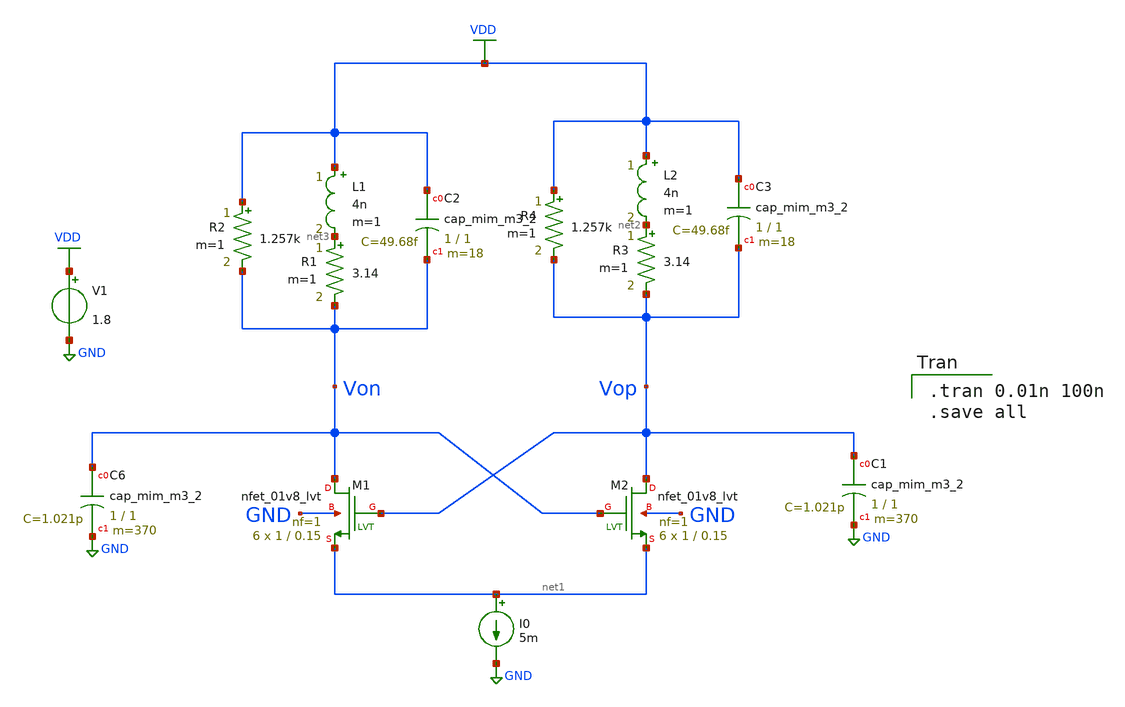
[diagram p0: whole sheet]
** sch_path: pll/lc_vco_lib/5_lc_vco_Hossam_Tarek/xschem/first_lc_osc.sch
**.subckt first_lc_osc
XM1 Von Vop net1 GND sky130_fd_pr__nfet_01v8_lvt L=0.15 W=1 nf=1 ad='int((nf+1)/2) * W/nf * 0.29' as='int((nf+2)/2) * W/nf * 0.29'
+ pd='2*int((nf+1)/2) * (W/nf + 0.29)' ps='2*int((nf+2)/2) * (W/nf + 0.29)' nrd='0.29 / W' nrs='0.29 / W'
+ sa=0 sb=0 sd=0 mult=6 m=6
XM2 Vop Von net1 GND sky130_fd_pr__nfet_01v8_lvt L=0.15 W=1 nf=1 ad='int((nf+1)/2) * W/nf * 0.29' as='int((nf+2)/2) * W/nf * 0.29'
+ pd='2*int((nf+1)/2) * (W/nf + 0.29)' ps='2*int((nf+2)/2) * (W/nf + 0.29)' nrd='0.29 / W' nrs='0.29 / W'
+ sa=0 sb=0 sd=0 mult=6 m=6
I0 net1 GND 5m
V1 VDD GND 1.8
L2 VDD net2 4n m=1
R3 net2 Vop 3.14 m=1
R4 VDD Vop 1.257k m=1
XC6 Von GND sky130_fd_pr__cap_mim_m3_2 W=1 L=1 MF=370 m=370
XC1 Vop GND sky130_fd_pr__cap_mim_m3_2 W=1 L=1 MF=370 m=370
XC3 VDD Vop sky130_fd_pr__cap_mim_m3_2 W=1 L=1 MF=18 m=18
L1 VDD net3 4n m=1
R1 net3 Von 3.14 m=1
R2 VDD Von 1.257k m=1
XC2 VDD Von sky130_fd_pr__cap_mim_m3_2 W=1 L=1 MF=18 m=18
**** begin user architecture code

.tran 0.01n 100n
.save all


** opencircuitdesign pdks install
.lib $::SKYWATER_MODELS/sky130.lib.spice tt


**** end user architecture code
**.ends
.GLOBAL GND
.GLOBAL VDD
.end
